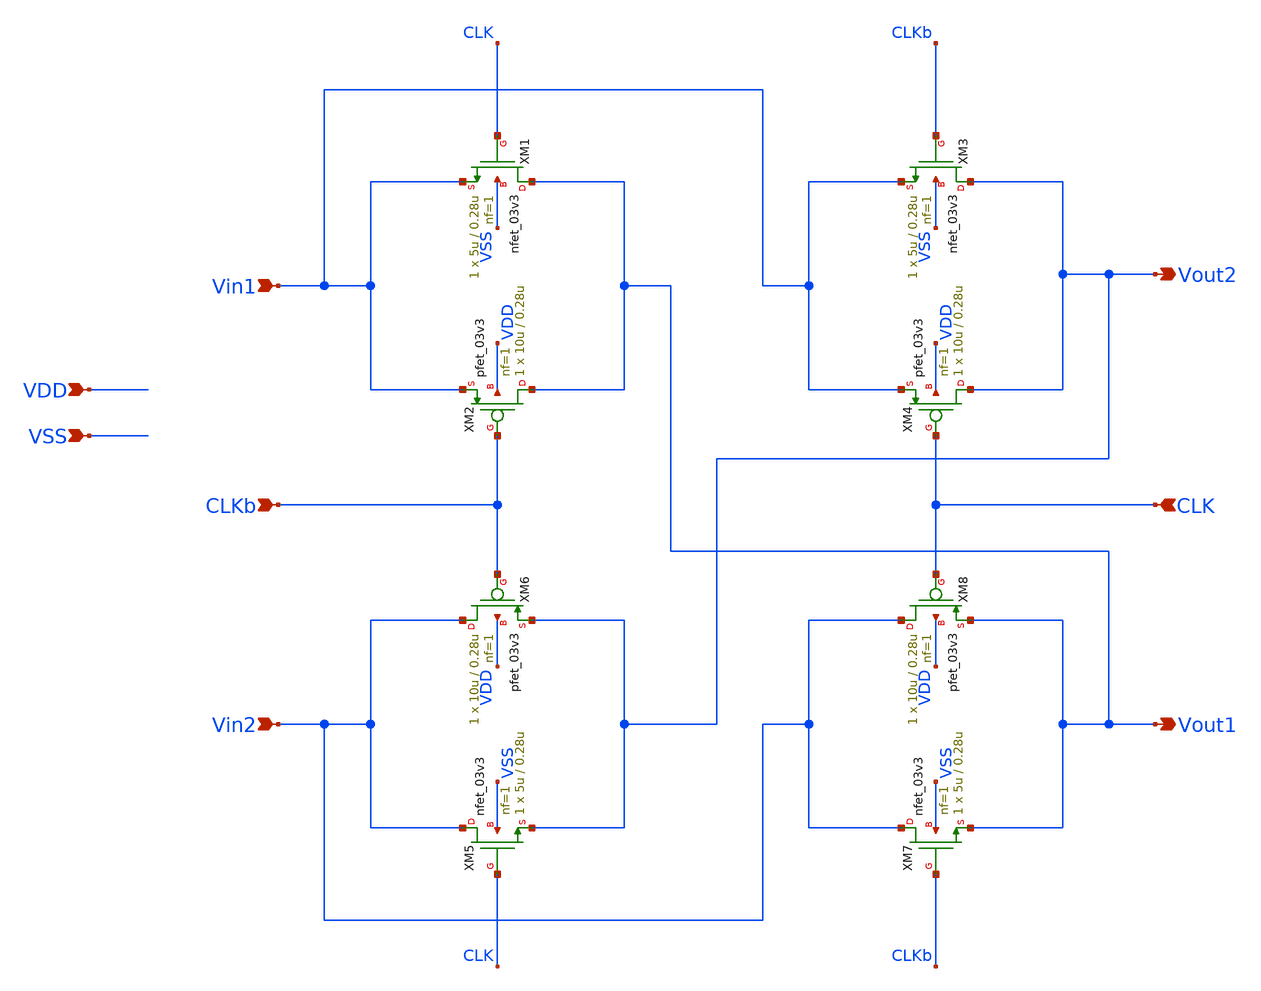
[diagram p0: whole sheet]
** sch_path: designs/libs/core_ina/ina_chopper/ina_chopper.sch
**.subckt ina_chopper Vin1 Vin2 CLKb Vout2 CLK Vout1 VDD VSS
*.ipin Vin1
*.ipin Vin2
*.ipin CLKb
*.opin Vout2
*.ipin CLK
*.opin Vout1
*.ipin VDD
*.ipin VSS
XM1 Vout1 CLK Vin1 VSS nfet_03v3 L=0.28u W=5u nf=1 ad='int((nf+1)/2) * W/nf * 0.18u' as='int((nf+2)/2) * W/nf * 0.18u'
+ pd='2*int((nf+1)/2) * (W/nf + 0.18u)' ps='2*int((nf+2)/2) * (W/nf + 0.18u)' nrd='0.18u / W' nrs='0.18u / W'
+ sa=0 sb=0 sd=0 m=1
XM2 Vout1 CLKb Vin1 VDD pfet_03v3 L=0.28u W=10u nf=1 ad='int((nf+1)/2) * W/nf * 0.18u' as='int((nf+2)/2) * W/nf * 0.18u'
+ pd='2*int((nf+1)/2) * (W/nf + 0.18u)' ps='2*int((nf+2)/2) * (W/nf + 0.18u)' nrd='0.18u / W' nrs='0.18u / W'
+ sa=0 sb=0 sd=0 m=1
XM3 Vout2 CLKb Vin1 VSS nfet_03v3 L=0.28u W=5u nf=1 ad='int((nf+1)/2) * W/nf * 0.18u' as='int((nf+2)/2) * W/nf * 0.18u'
+ pd='2*int((nf+1)/2) * (W/nf + 0.18u)' ps='2*int((nf+2)/2) * (W/nf + 0.18u)' nrd='0.18u / W' nrs='0.18u / W'
+ sa=0 sb=0 sd=0 m=1
XM4 Vout2 CLK Vin1 VDD pfet_03v3 L=0.28u W=10u nf=1 ad='int((nf+1)/2) * W/nf * 0.18u' as='int((nf+2)/2) * W/nf * 0.18u'
+ pd='2*int((nf+1)/2) * (W/nf + 0.18u)' ps='2*int((nf+2)/2) * (W/nf + 0.18u)' nrd='0.18u / W' nrs='0.18u / W'
+ sa=0 sb=0 sd=0 m=1
XM5 Vin2 CLK Vout2 VSS nfet_03v3 L=0.28u W=5u nf=1 ad='int((nf+1)/2) * W/nf * 0.18u' as='int((nf+2)/2) * W/nf * 0.18u'
+ pd='2*int((nf+1)/2) * (W/nf + 0.18u)' ps='2*int((nf+2)/2) * (W/nf + 0.18u)' nrd='0.18u / W' nrs='0.18u / W'
+ sa=0 sb=0 sd=0 m=1
XM6 Vin2 CLKb Vout2 VDD pfet_03v3 L=0.28u W=10u nf=1 ad='int((nf+1)/2) * W/nf * 0.18u' as='int((nf+2)/2) * W/nf * 0.18u'
+ pd='2*int((nf+1)/2) * (W/nf + 0.18u)' ps='2*int((nf+2)/2) * (W/nf + 0.18u)' nrd='0.18u / W' nrs='0.18u / W'
+ sa=0 sb=0 sd=0 m=1
XM7 Vin2 CLKb Vout1 VSS nfet_03v3 L=0.28u W=5u nf=1 ad='int((nf+1)/2) * W/nf * 0.18u' as='int((nf+2)/2) * W/nf * 0.18u'
+ pd='2*int((nf+1)/2) * (W/nf + 0.18u)' ps='2*int((nf+2)/2) * (W/nf + 0.18u)' nrd='0.18u / W' nrs='0.18u / W'
+ sa=0 sb=0 sd=0 m=1
XM8 Vin2 CLK Vout1 VDD pfet_03v3 L=0.28u W=10u nf=1 ad='int((nf+1)/2) * W/nf * 0.18u' as='int((nf+2)/2) * W/nf * 0.18u'
+ pd='2*int((nf+1)/2) * (W/nf + 0.18u)' ps='2*int((nf+2)/2) * (W/nf + 0.18u)' nrd='0.18u / W' nrs='0.18u / W'
+ sa=0 sb=0 sd=0 m=1
**.ends
.end
